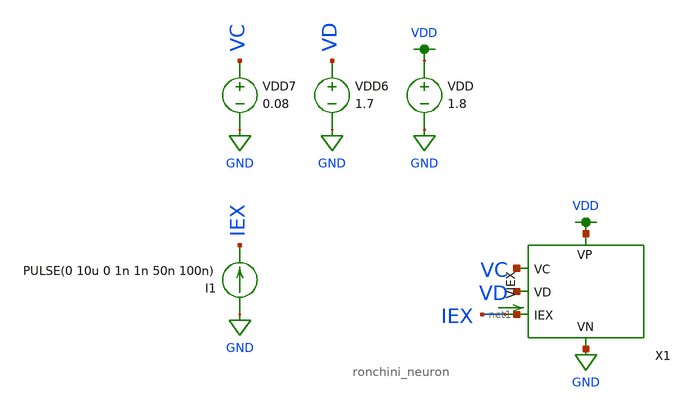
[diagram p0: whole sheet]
** sch_path: schematic/ronchini_neuron_tran.sch
**.subckt ronchini_neuron_tran
VDD VDD GND 1.8
I1 GND IEX PULSE(0 10u 0 1n 1n 50n 100n)
VDD6 VD GND 1.7
VDD7 VC GND 0.08
X1 VC VD net1 GND VDD ronchini_neuron
VIEX IEX net1 0
.save i(viex)
**** begin user architecture code

.param W=12
.param L=0.5
.tran 0.1n 250n
.save all


.option wnflag=1
.param MC_SWITCH=0.0
.lib ~/skywater/skywater-pdk/libraries/sky130_fd_pr_ngspice/latest/models/sky130.lib.spice tt

**** end user architecture code
**.ends

* expanding   symbol:
*+  /home/madvlsi/Documents/neuromorphic_computing_final/schematic/ronchini_neuron.sym # of pins=5
** sym_path: schematic/ronchini_neuron.sym
** sch_path: schematic/ronchini_neuron.sch
.subckt ronchini_neuron VC VD IEX VN VP
*.iopin VN
*.iopin VP
*.ipin IEX
*.iopin VD
*.iopin VC
CV IEX VN 35f m=1
CU net2 VN 550f m=1
XM7 net2 net1 VP VDD sky130_fd_pr__pfet_01v8 L=0.15 W=1 nf=1 ad='int((nf+1)/2) * W/nf * 0.29' as='int((nf+2)/2) * W/nf * 0.29'
+ pd='2*int((nf+1)/2) * (W/nf + 0.29)' ps='2*int((nf+2)/2) * (W/nf + 0.29)' nrd='0.29 / W' nrs='0.29 / W'
+ sa=0 sb=0 sd=0 mult=0.5 m=0.5
XM8 VD net3 net2 VDD sky130_fd_pr__pfet_01v8 L=0.15 W=1 nf=1 ad='int((nf+1)/2) * W/nf * 0.29' as='int((nf+2)/2) * W/nf * 0.29'
+ pd='2*int((nf+1)/2) * (W/nf + 0.29)' ps='2*int((nf+2)/2) * (W/nf + 0.29)' nrd='0.29 / W' nrs='0.29 / W'
+ sa=0 sb=0 sd=0 mult=10.4 m=10.4
XM10 net3 IEX VN GND sky130_fd_pr__nfet_01v8 L=0.15 W=1 nf=1 ad='int((nf+1)/2) * W/nf * 0.29' as='int((nf+2)/2) * W/nf * 0.29'
+ pd='2*int((nf+1)/2) * (W/nf + 0.29)' ps='2*int((nf+2)/2) * (W/nf + 0.29)' nrd='0.29 / W' nrs='0.29 / W'
+ sa=0 sb=0 sd=0 mult=1.2 m=1.2
XM12 VN net3 comp_out GND sky130_fd_pr__nfet_01v8 L=0.15 W=1 nf=1 ad='int((nf+1)/2) * W/nf * 0.29' as='int((nf+2)/2) * W/nf * 0.29'
+ pd='2*int((nf+1)/2) * (W/nf + 0.29)' ps='2*int((nf+2)/2) * (W/nf + 0.29)' nrd='0.29 / W' nrs='0.29 / W'
+ sa=0 sb=0 sd=0 mult=1.2 m=1.2
XM5 VC comp_out IEX GND sky130_fd_pr__nfet_01v8 L=0.15 W=1 nf=1 ad='int((nf+1)/2) * W/nf * 0.29' as='int((nf+2)/2) * W/nf * 0.29'
+ pd='2*int((nf+1)/2) * (W/nf + 0.29)' ps='2*int((nf+2)/2) * (W/nf + 0.29)' nrd='0.29 / W' nrs='0.29 / W'
+ sa=0 sb=0 sd=0 mult=1.9 m=1.9
XM2 VP net1 net1 VDD sky130_fd_pr__pfet_01v8 L=0.15 W=1 nf=1 ad='int((nf+1)/2) * W/nf * 0.29' as='int((nf+2)/2) * W/nf * 0.29'
+ pd='2*int((nf+1)/2) * (W/nf + 0.29)' ps='2*int((nf+2)/2) * (W/nf + 0.29)' nrd='0.29 / W' nrs='0.29 / W'
+ sa=0 sb=0 sd=0 mult=2.3 m=2.3
XM3 VP net1 IEX VDD sky130_fd_pr__pfet_01v8 L=0.15 W=1 nf=1 ad='int((nf+1)/2) * W/nf * 0.29' as='int((nf+2)/2) * W/nf * 0.29'
+ pd='2*int((nf+1)/2) * (W/nf + 0.29)' ps='2*int((nf+2)/2) * (W/nf + 0.29)' nrd='0.29 / W' nrs='0.29 / W'
+ sa=0 sb=0 sd=0 mult=2.3 m=2.3
XM1 VN IEX net1 GND sky130_fd_pr__nfet_01v8 L=0.15 W=1 nf=1 ad='int((nf+1)/2) * W/nf * 0.29' as='int((nf+2)/2) * W/nf * 0.29'
+ pd='2*int((nf+1)/2) * (W/nf + 0.29)' ps='2*int((nf+2)/2) * (W/nf + 0.29)' nrd='0.29 / W' nrs='0.29 / W'
+ sa=0 sb=0 sd=0 mult=2.3 m=2.3
XM4 VN net2 IEX GND sky130_fd_pr__nfet_01v8 L=0.15 W=1 nf=1 ad='int((nf+1)/2) * W/nf * 0.29' as='int((nf+2)/2) * W/nf * 0.29'
+ pd='2*int((nf+1)/2) * (W/nf + 0.29)' ps='2*int((nf+2)/2) * (W/nf + 0.29)' nrd='0.29 / W' nrs='0.29 / W'
+ sa=0 sb=0 sd=0 mult=10.5 m=10.5
XM6 VN net2 net2 GND sky130_fd_pr__nfet_01v8 L=0.15 W=1 nf=1 ad='int((nf+1)/2) * W/nf * 0.29' as='int((nf+2)/2) * W/nf * 0.29'
+ pd='2*int((nf+1)/2) * (W/nf + 0.29)' ps='2*int((nf+2)/2) * (W/nf + 0.29)' nrd='0.29 / W' nrs='0.29 / W'
+ sa=0 sb=0 sd=0 mult=5.5 m=5.5
XM9 net3 IEX VP VDD sky130_fd_pr__pfet_01v8 L=0.15 W=1 nf=1 ad='int((nf+1)/2) * W/nf * 0.29' as='int((nf+2)/2) * W/nf * 0.29'
+ pd='2*int((nf+1)/2) * (W/nf + 0.29)' ps='2*int((nf+2)/2) * (W/nf + 0.29)' nrd='0.29 / W' nrs='0.29 / W'
+ sa=0 sb=0 sd=0 mult=12.2 m=12.2
XM11 VP net3 comp_out VDD sky130_fd_pr__pfet_01v8 L=0.15 W=1 nf=1 ad='int((nf+1)/2) * W/nf * 0.29' as='int((nf+2)/2) * W/nf * 0.29'
+ pd='2*int((nf+1)/2) * (W/nf + 0.29)' ps='2*int((nf+2)/2) * (W/nf + 0.29)' nrd='0.29 / W' nrs='0.29 / W'
+ sa=0 sb=0 sd=0 mult=12.2 m=12.2
.ends

.GLOBAL GND
.GLOBAL VDD
.end
